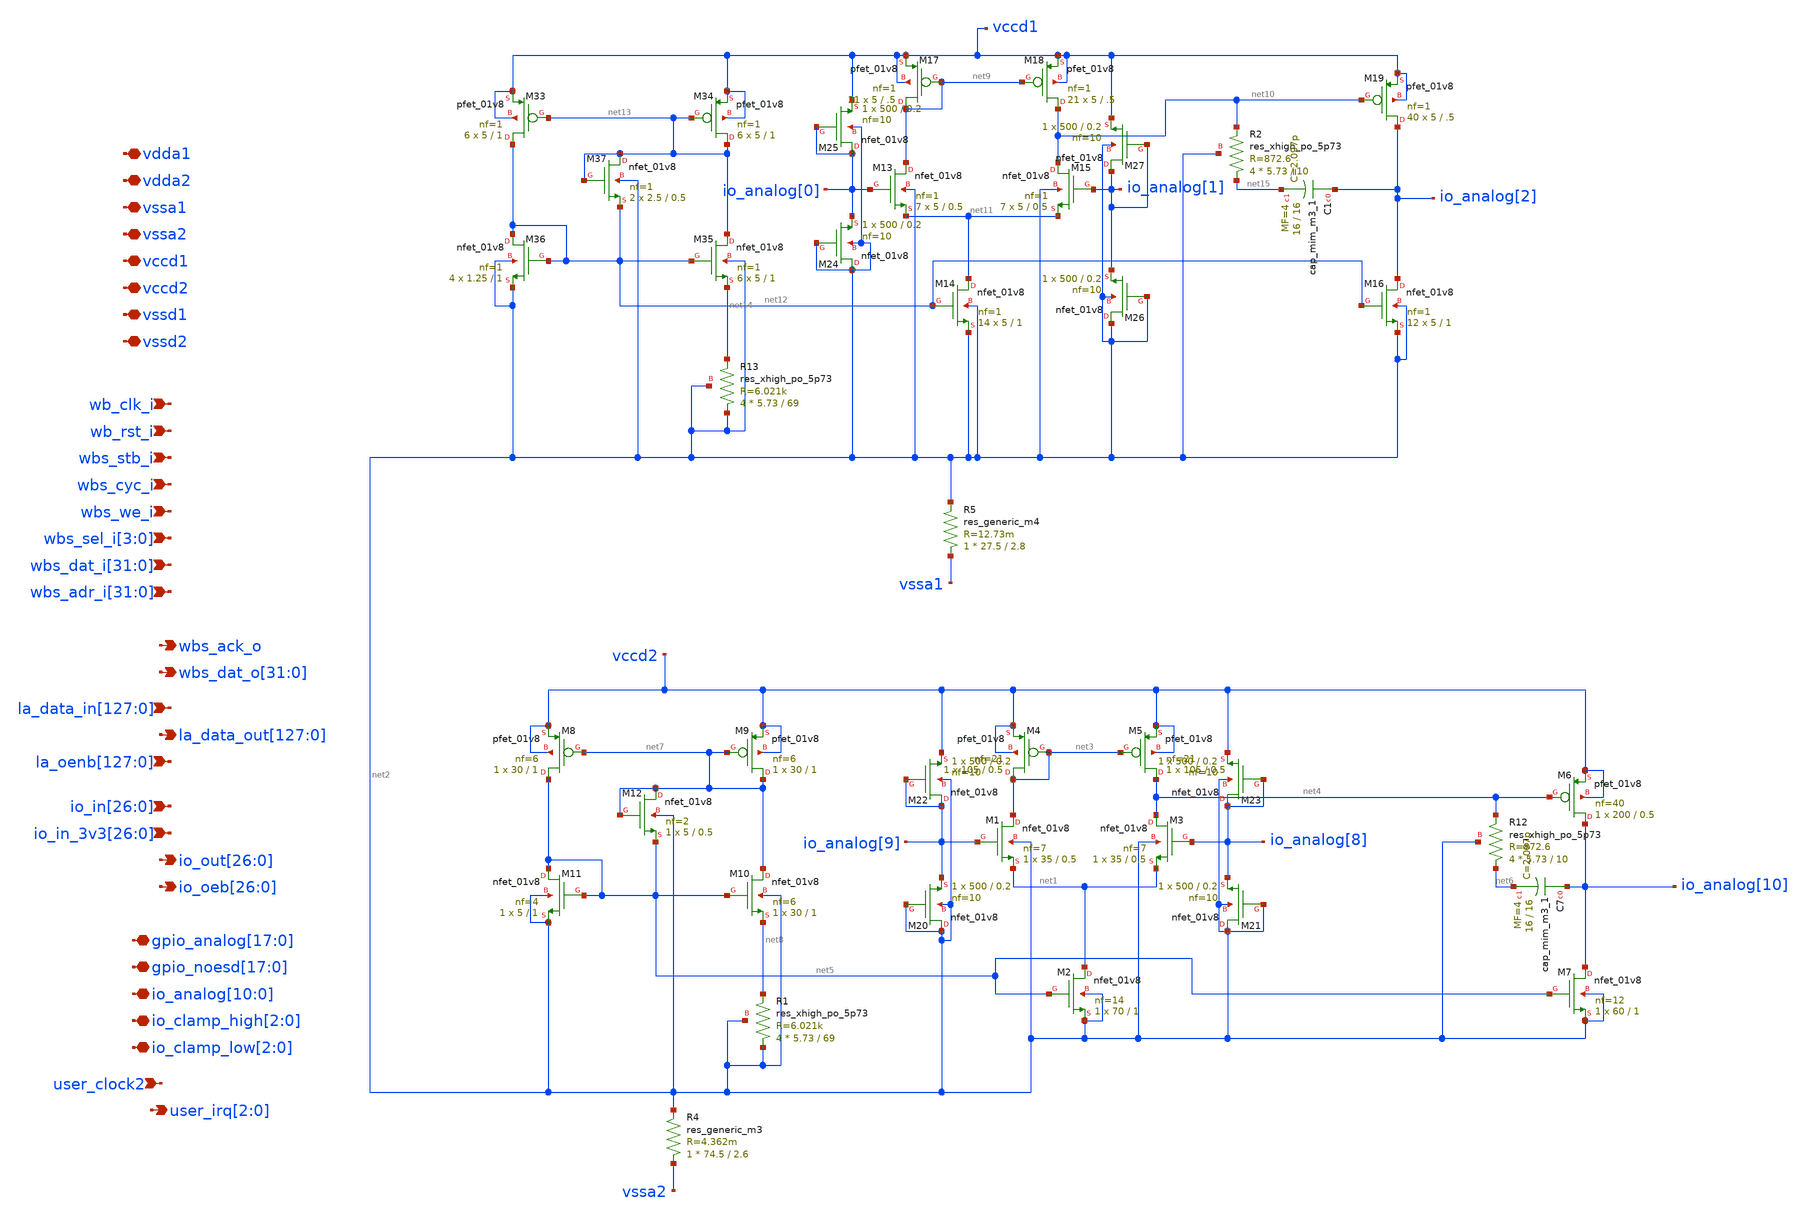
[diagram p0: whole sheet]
** sch_path: xschem/user_analog_project_wrapper.sch
**.subckt user_analog_project_wrapper vdda1 vdda2 vssa1 vssa2 vccd1 vccd2 vssd1 vssd2 wb_clk_i
*+ wb_rst_i wbs_stb_i wbs_cyc_i wbs_we_i wbs_sel_i[3],wbs_sel_i[2],wbs_sel_i[1],wbs_sel_i[0]
*+ wbs_dat_i[31],wbs_dat_i[30],wbs_dat_i[29],wbs_dat_i[28],wbs_dat_i[27],wbs_dat_i[26],wbs_dat_i[25],wbs_dat_i[24],wbs_dat_i[23],wbs_dat_i[22],wbs_dat_i[21],wbs_dat_i[20],wbs_dat_i[19],wbs_dat_i[18],wbs_dat_i[17],wbs_dat_i[16],wbs_dat_i[15],wbs_dat_i[14],wbs_dat_i[13],wbs_dat_i[12],wbs_dat_i[11],wbs_dat_i[10],wbs_dat_i[9],wbs_dat_i[8],wbs_dat_i[7],wbs_dat_i[6],wbs_dat_i[5],wbs_dat_i[4],wbs_dat_i[3],wbs_dat_i[2],wbs_dat_i[1],wbs_dat_i[0]
*+ wbs_adr_i[31],wbs_adr_i[30],wbs_adr_i[29],wbs_adr_i[28],wbs_adr_i[27],wbs_adr_i[26],wbs_adr_i[25],wbs_adr_i[24],wbs_adr_i[23],wbs_adr_i[22],wbs_adr_i[21],wbs_adr_i[20],wbs_adr_i[19],wbs_adr_i[18],wbs_adr_i[17],wbs_adr_i[16],wbs_adr_i[15],wbs_adr_i[14],wbs_adr_i[13],wbs_adr_i[12],wbs_adr_i[11],wbs_adr_i[10],wbs_adr_i[9],wbs_adr_i[8],wbs_adr_i[7],wbs_adr_i[6],wbs_adr_i[5],wbs_adr_i[4],wbs_adr_i[3],wbs_adr_i[2],wbs_adr_i[1],wbs_adr_i[0] wbs_ack_o
*+ wbs_dat_o[31],wbs_dat_o[30],wbs_dat_o[29],wbs_dat_o[28],wbs_dat_o[27],wbs_dat_o[26],wbs_dat_o[25],wbs_dat_o[24],wbs_dat_o[23],wbs_dat_o[22],wbs_dat_o[21],wbs_dat_o[20],wbs_dat_o[19],wbs_dat_o[18],wbs_dat_o[17],wbs_dat_o[16],wbs_dat_o[15],wbs_dat_o[14],wbs_dat_o[13],wbs_dat_o[12],wbs_dat_o[11],wbs_dat_o[10],wbs_dat_o[9],wbs_dat_o[8],wbs_dat_o[7],wbs_dat_o[6],wbs_dat_o[5],wbs_dat_o[4],wbs_dat_o[3],wbs_dat_o[2],wbs_dat_o[1],wbs_dat_o[0]
*+ la_data_in[127],la_data_in[126],la_data_in[125],la_data_in[124],la_data_in[123],la_data_in[122],la_data_in[121],la_data_in[120],la_data_in[119],la_data_in[118],la_data_in[117],la_data_in[116],la_data_in[115],la_data_in[114],la_data_in[113],la_data_in[112],la_data_in[111],la_data_in[110],la_data_in[109],la_data_in[108],la_data_in[107],la_data_in[106],la_data_in[105],la_data_in[104],la_data_in[103],la_data_in[102],la_data_in[101],la_data_in[100],la_data_in[99],la_data_in[98],la_data_in[97],la_data_in[96],la_data_in[95],la_data_in[94],la_data_in[93],la_data_in[92],la_data_in[91],la_data_in[90],la_data_in[89],la_data_in[88],la_data_in[87],la_data_in[86],la_data_in[85],la_data_in[84],la_data_in[83],la_data_in[82],la_data_in[81],la_data_in[80],la_data_in[79],la_data_in[78],la_data_in[77],la_data_in[76],la_data_in[75],la_data_in[74],la_data_in[73],la_data_in[72],la_data_in[71],la_data_in[70],la_data_in[69],la_data_in[68],la_data_in[67],la_data_in[66],la_data_in[65],la_data_in[64],la_data_in[63],la_data_in[62],la_data_in[61],la_data_in[60],la_data_in[59],la_data_in[58],la_data_in[57],la_data_in[56],la_data_in[55],la_data_in[54],la_data_in[53],la_data_in[52],la_data_in[51],la_data_in[50],la_data_in[49],la_data_in[48],la_data_in[47],la_data_in[46],la_data_in[45],la_data_in[44],la_data_in[43],la_data_in[42],la_data_in[41],la_data_in[40],la_data_in[39],la_data_in[38],la_data_in[37],la_data_in[36],la_data_in[35],la_data_in[34],la_data_in[33],la_data_in[32],la_data_in[31],la_data_in[30],la_data_in[29],la_data_in[28],la_data_in[27],la_data_in[26],la_data_in[25],la_data_in[24],la_data_in[23],la_data_in[22],la_data_in[21],la_data_in[20],la_data_in[19],la_data_in[18],la_data_in[17],la_data_in[16],la_data_in[15],la_data_in[14],la_data_in[13],la_data_in[12],la_data_in[11],la_data_in[10],la_data_in[9],la_data_in[8],la_data_in[7],la_data_in[6],la_data_in[5],la_data_in[4],la_data_in[3],la_data_in[2],la_data_in[1],la_data_in[0]
*+ la_data_out[127],la_data_out[126],la_data_out[125],la_data_out[124],la_data_out[123],la_data_out[122],la_data_out[121],la_data_out[120],la_data_out[119],la_data_out[118],la_data_out[117],la_data_out[116],la_data_out[115],la_data_out[114],la_data_out[113],la_data_out[112],la_data_out[111],la_data_out[110],la_data_out[109],la_data_out[108],la_data_out[107],la_data_out[106],la_data_out[105],la_data_out[104],la_data_out[103],la_data_out[102],la_data_out[101],la_data_out[100],la_data_out[99],la_data_out[98],la_data_out[97],la_data_out[96],la_data_out[95],la_data_out[94],la_data_out[93],la_data_out[92],la_data_out[91],la_data_out[90],la_data_out[89],la_data_out[88],la_data_out[87],la_data_out[86],la_data_out[85],la_data_out[84],la_data_out[83],la_data_out[82],la_data_out[81],la_data_out[80],la_data_out[79],la_data_out[78],la_data_out[77],la_data_out[76],la_data_out[75],la_data_out[74],la_data_out[73],la_data_out[72],la_data_out[71],la_data_out[70],la_data_out[69],la_data_out[68],la_data_out[67],la_data_out[66],la_data_out[65],la_data_out[64],la_data_out[63],la_data_out[62],la_data_out[61],la_data_out[60],la_data_out[59],la_data_out[58],la_data_out[57],la_data_out[56],la_data_out[55],la_data_out[54],la_data_out[53],la_data_out[52],la_data_out[51],la_data_out[50],la_data_out[49],la_data_out[48],la_data_out[47],la_data_out[46],la_data_out[45],la_data_out[44],la_data_out[43],la_data_out[42],la_data_out[41],la_data_out[40],la_data_out[39],la_data_out[38],la_data_out[37],la_data_out[36],la_data_out[35],la_data_out[34],la_data_out[33],la_data_out[32],la_data_out[31],la_data_out[30],la_data_out[29],la_data_out[28],la_data_out[27],la_data_out[26],la_data_out[25],la_data_out[24],la_data_out[23],la_data_out[22],la_data_out[21],la_data_out[20],la_data_out[19],la_data_out[18],la_data_out[17],la_data_out[16],la_data_out[15],la_data_out[14],la_data_out[13],la_data_out[12],la_data_out[11],la_data_out[10],la_data_out[9],la_data_out[8],la_data_out[7],la_data_out[6],la_data_out[5],la_data_out[4],la_data_out[3],la_data_out[2],la_data_out[1],la_data_out[0]
*+ io_in[26],io_in[25],io_in[24],io_in[23],io_in[22],io_in[21],io_in[20],io_in[19],io_in[18],io_in[17],io_in[16],io_in[15],io_in[14],io_in[13],io_in[12],io_in[11],io_in[10],io_in[9],io_in[8],io_in[7],io_in[6],io_in[5],io_in[4],io_in[3],io_in[2],io_in[1],io_in[0]
*+ io_in_3v3[26],io_in_3v3[25],io_in_3v3[24],io_in_3v3[23],io_in_3v3[22],io_in_3v3[21],io_in_3v3[20],io_in_3v3[19],io_in_3v3[18],io_in_3v3[17],io_in_3v3[16],io_in_3v3[15],io_in_3v3[14],io_in_3v3[13],io_in_3v3[12],io_in_3v3[11],io_in_3v3[10],io_in_3v3[9],io_in_3v3[8],io_in_3v3[7],io_in_3v3[6],io_in_3v3[5],io_in_3v3[4],io_in_3v3[3],io_in_3v3[2],io_in_3v3[1],io_in_3v3[0] user_clock2
*+ io_out[26],io_out[25],io_out[24],io_out[23],io_out[22],io_out[21],io_out[20],io_out[19],io_out[18],io_out[17],io_out[16],io_out[15],io_out[14],io_out[13],io_out[12],io_out[11],io_out[10],io_out[9],io_out[8],io_out[7],io_out[6],io_out[5],io_out[4],io_out[3],io_out[2],io_out[1],io_out[0]
*+ io_oeb[26],io_oeb[25],io_oeb[24],io_oeb[23],io_oeb[22],io_oeb[21],io_oeb[20],io_oeb[19],io_oeb[18],io_oeb[17],io_oeb[16],io_oeb[15],io_oeb[14],io_oeb[13],io_oeb[12],io_oeb[11],io_oeb[10],io_oeb[9],io_oeb[8],io_oeb[7],io_oeb[6],io_oeb[5],io_oeb[4],io_oeb[3],io_oeb[2],io_oeb[1],io_oeb[0]
*+ gpio_analog[17],gpio_analog[16],gpio_analog[15],gpio_analog[14],gpio_analog[13],gpio_analog[12],gpio_analog[11],gpio_analog[10],gpio_analog[9],gpio_analog[8],gpio_analog[7],gpio_analog[6],gpio_analog[5],gpio_analog[4],gpio_analog[3],gpio_analog[2],gpio_analog[1],gpio_analog[0]
*+ gpio_noesd[17],gpio_noesd[16],gpio_noesd[15],gpio_noesd[14],gpio_noesd[13],gpio_noesd[12],gpio_noesd[11],gpio_noesd[10],gpio_noesd[9],gpio_noesd[8],gpio_noesd[7],gpio_noesd[6],gpio_noesd[5],gpio_noesd[4],gpio_noesd[3],gpio_noesd[2],gpio_noesd[1],gpio_noesd[0]
*+ io_analog[10],io_analog[9],io_analog[8],io_analog[7],io_analog[6],io_analog[5],io_analog[4],io_analog[3],io_analog[2],io_analog[1],io_analog[0] io_clamp_high[2],io_clamp_high[1],io_clamp_high[0] io_clamp_low[2],io_clamp_low[1],io_clamp_low[0]
*+ user_irq[2],user_irq[1],user_irq[0]
*+ la_oenb[127],la_oenb[126],la_oenb[125],la_oenb[124],la_oenb[123],la_oenb[122],la_oenb[121],la_oenb[120],la_oenb[119],la_oenb[118],la_oenb[117],la_oenb[116],la_oenb[115],la_oenb[114],la_oenb[113],la_oenb[112],la_oenb[111],la_oenb[110],la_oenb[109],la_oenb[108],la_oenb[107],la_oenb[106],la_oenb[105],la_oenb[104],la_oenb[103],la_oenb[102],la_oenb[101],la_oenb[100],la_oenb[99],la_oenb[98],la_oenb[97],la_oenb[96],la_oenb[95],la_oenb[94],la_oenb[93],la_oenb[92],la_oenb[91],la_oenb[90],la_oenb[89],la_oenb[88],la_oenb[87],la_oenb[86],la_oenb[85],la_oenb[84],la_oenb[83],la_oenb[82],la_oenb[81],la_oenb[80],la_oenb[79],la_oenb[78],la_oenb[77],la_oenb[76],la_oenb[75],la_oenb[74],la_oenb[73],la_oenb[72],la_oenb[71],la_oenb[70],la_oenb[69],la_oenb[68],la_oenb[67],la_oenb[66],la_oenb[65],la_oenb[64],la_oenb[63],la_oenb[62],la_oenb[61],la_oenb[60],la_oenb[59],la_oenb[58],la_oenb[57],la_oenb[56],la_oenb[55],la_oenb[54],la_oenb[53],la_oenb[52],la_oenb[51],la_oenb[50],la_oenb[49],la_oenb[48],la_oenb[47],la_oenb[46],la_oenb[45],la_oenb[44],la_oenb[43],la_oenb[42],la_oenb[41],la_oenb[40],la_oenb[39],la_oenb[38],la_oenb[37],la_oenb[36],la_oenb[35],la_oenb[34],la_oenb[33],la_oenb[32],la_oenb[31],la_oenb[30],la_oenb[29],la_oenb[28],la_oenb[27],la_oenb[26],la_oenb[25],la_oenb[24],la_oenb[23],la_oenb[22],la_oenb[21],la_oenb[20],la_oenb[19],la_oenb[18],la_oenb[17],la_oenb[16],la_oenb[15],la_oenb[14],la_oenb[13],la_oenb[12],la_oenb[11],la_oenb[10],la_oenb[9],la_oenb[8],la_oenb[7],la_oenb[6],la_oenb[5],la_oenb[4],la_oenb[3],la_oenb[2],la_oenb[1],la_oenb[0]
*.iopin vdda1
*.iopin vdda2
*.iopin vssa1
*.iopin vssa2
*.iopin vccd1
*.iopin vccd2
*.iopin vssd1
*.iopin vssd2
*.ipin wb_clk_i
*.ipin wb_rst_i
*.ipin wbs_stb_i
*.ipin wbs_cyc_i
*.ipin wbs_we_i
*.ipin wbs_sel_i[3],wbs_sel_i[2],wbs_sel_i[1],wbs_sel_i[0]
*.ipin
*+ wbs_dat_i[31],wbs_dat_i[30],wbs_dat_i[29],wbs_dat_i[28],wbs_dat_i[27],wbs_dat_i[26],wbs_dat_i[25],wbs_dat_i[24],wbs_dat_i[23],wbs_dat_i[22],wbs_dat_i[21],wbs_dat_i[20],wbs_dat_i[19],wbs_dat_i[18],wbs_dat_i[17],wbs_dat_i[16],wbs_dat_i[15],wbs_dat_i[14],wbs_dat_i[13],wbs_dat_i[12],wbs_dat_i[11],wbs_dat_i[10],wbs_dat_i[9],wbs_dat_i[8],wbs_dat_i[7],wbs_dat_i[6],wbs_dat_i[5],wbs_dat_i[4],wbs_dat_i[3],wbs_dat_i[2],wbs_dat_i[1],wbs_dat_i[0]
*.ipin
*+ wbs_adr_i[31],wbs_adr_i[30],wbs_adr_i[29],wbs_adr_i[28],wbs_adr_i[27],wbs_adr_i[26],wbs_adr_i[25],wbs_adr_i[24],wbs_adr_i[23],wbs_adr_i[22],wbs_adr_i[21],wbs_adr_i[20],wbs_adr_i[19],wbs_adr_i[18],wbs_adr_i[17],wbs_adr_i[16],wbs_adr_i[15],wbs_adr_i[14],wbs_adr_i[13],wbs_adr_i[12],wbs_adr_i[11],wbs_adr_i[10],wbs_adr_i[9],wbs_adr_i[8],wbs_adr_i[7],wbs_adr_i[6],wbs_adr_i[5],wbs_adr_i[4],wbs_adr_i[3],wbs_adr_i[2],wbs_adr_i[1],wbs_adr_i[0]
*.opin wbs_ack_o
*.opin
*+ wbs_dat_o[31],wbs_dat_o[30],wbs_dat_o[29],wbs_dat_o[28],wbs_dat_o[27],wbs_dat_o[26],wbs_dat_o[25],wbs_dat_o[24],wbs_dat_o[23],wbs_dat_o[22],wbs_dat_o[21],wbs_dat_o[20],wbs_dat_o[19],wbs_dat_o[18],wbs_dat_o[17],wbs_dat_o[16],wbs_dat_o[15],wbs_dat_o[14],wbs_dat_o[13],wbs_dat_o[12],wbs_dat_o[11],wbs_dat_o[10],wbs_dat_o[9],wbs_dat_o[8],wbs_dat_o[7],wbs_dat_o[6],wbs_dat_o[5],wbs_dat_o[4],wbs_dat_o[3],wbs_dat_o[2],wbs_dat_o[1],wbs_dat_o[0]
*.ipin
*+ la_data_in[127],la_data_in[126],la_data_in[125],la_data_in[124],la_data_in[123],la_data_in[122],la_data_in[121],la_data_in[120],la_data_in[119],la_data_in[118],la_data_in[117],la_data_in[116],la_data_in[115],la_data_in[114],la_data_in[113],la_data_in[112],la_data_in[111],la_data_in[110],la_data_in[109],la_data_in[108],la_data_in[107],la_data_in[106],la_data_in[105],la_data_in[104],la_data_in[103],la_data_in[102],la_data_in[101],la_data_in[100],la_data_in[99],la_data_in[98],la_data_in[97],la_data_in[96],la_data_in[95],la_data_in[94],la_data_in[93],la_data_in[92],la_data_in[91],la_data_in[90],la_data_in[89],la_data_in[88],la_data_in[87],la_data_in[86],la_data_in[85],la_data_in[84],la_data_in[83],la_data_in[82],la_data_in[81],la_data_in[80],la_data_in[79],la_data_in[78],la_data_in[77],la_data_in[76],la_data_in[75],la_data_in[74],la_data_in[73],la_data_in[72],la_data_in[71],la_data_in[70],la_data_in[69],la_data_in[68],la_data_in[67],la_data_in[66],la_data_in[65],la_data_in[64],la_data_in[63],la_data_in[62],la_data_in[61],la_data_in[60],la_data_in[59],la_data_in[58],la_data_in[57],la_data_in[56],la_data_in[55],la_data_in[54],la_data_in[53],la_data_in[52],la_data_in[51],la_data_in[50],la_data_in[49],la_data_in[48],la_data_in[47],la_data_in[46],la_data_in[45],la_data_in[44],la_data_in[43],la_data_in[42],la_data_in[41],la_data_in[40],la_data_in[39],la_data_in[38],la_data_in[37],la_data_in[36],la_data_in[35],la_data_in[34],la_data_in[33],la_data_in[32],la_data_in[31],la_data_in[30],la_data_in[29],la_data_in[28],la_data_in[27],la_data_in[26],la_data_in[25],la_data_in[24],la_data_in[23],la_data_in[22],la_data_in[21],la_data_in[20],la_data_in[19],la_data_in[18],la_data_in[17],la_data_in[16],la_data_in[15],la_data_in[14],la_data_in[13],la_data_in[12],la_data_in[11],la_data_in[10],la_data_in[9],la_data_in[8],la_data_in[7],la_data_in[6],la_data_in[5],la_data_in[4],la_data_in[3],la_data_in[2],la_data_in[1],la_data_in[0]
*.opin
*+ la_data_out[127],la_data_out[126],la_data_out[125],la_data_out[124],la_data_out[123],la_data_out[122],la_data_out[121],la_data_out[120],la_data_out[119],la_data_out[118],la_data_out[117],la_data_out[116],la_data_out[115],la_data_out[114],la_data_out[113],la_data_out[112],la_data_out[111],la_data_out[110],la_data_out[109],la_data_out[108],la_data_out[107],la_data_out[106],la_data_out[105],la_data_out[104],la_data_out[103],la_data_out[102],la_data_out[101],la_data_out[100],la_data_out[99],la_data_out[98],la_data_out[97],la_data_out[96],la_data_out[95],la_data_out[94],la_data_out[93],la_data_out[92],la_data_out[91],la_data_out[90],la_data_out[89],la_data_out[88],la_data_out[87],la_data_out[86],la_data_out[85],la_data_out[84],la_data_out[83],la_data_out[82],la_data_out[81],la_data_out[80],la_data_out[79],la_data_out[78],la_data_out[77],la_data_out[76],la_data_out[75],la_data_out[74],la_data_out[73],la_data_out[72],la_data_out[71],la_data_out[70],la_data_out[69],la_data_out[68],la_data_out[67],la_data_out[66],la_data_out[65],la_data_out[64],la_data_out[63],la_data_out[62],la_data_out[61],la_data_out[60],la_data_out[59],la_data_out[58],la_data_out[57],la_data_out[56],la_data_out[55],la_data_out[54],la_data_out[53],la_data_out[52],la_data_out[51],la_data_out[50],la_data_out[49],la_data_out[48],la_data_out[47],la_data_out[46],la_data_out[45],la_data_out[44],la_data_out[43],la_data_out[42],la_data_out[41],la_data_out[40],la_data_out[39],la_data_out[38],la_data_out[37],la_data_out[36],la_data_out[35],la_data_out[34],la_data_out[33],la_data_out[32],la_data_out[31],la_data_out[30],la_data_out[29],la_data_out[28],la_data_out[27],la_data_out[26],la_data_out[25],la_data_out[24],la_data_out[23],la_data_out[22],la_data_out[21],la_data_out[20],la_data_out[19],la_data_out[18],la_data_out[17],la_data_out[16],la_data_out[15],la_data_out[14],la_data_out[13],la_data_out[12],la_data_out[11],la_data_out[10],la_data_out[9],la_data_out[8],la_data_out[7],la_data_out[6],la_data_out[5],la_data_out[4],la_data_out[3],la_data_out[2],la_data_out[1],la_data_out[0]
*.ipin
*+ io_in[26],io_in[25],io_in[24],io_in[23],io_in[22],io_in[21],io_in[20],io_in[19],io_in[18],io_in[17],io_in[16],io_in[15],io_in[14],io_in[13],io_in[12],io_in[11],io_in[10],io_in[9],io_in[8],io_in[7],io_in[6],io_in[5],io_in[4],io_in[3],io_in[2],io_in[1],io_in[0]
*.ipin
*+ io_in_3v3[26],io_in_3v3[25],io_in_3v3[24],io_in_3v3[23],io_in_3v3[22],io_in_3v3[21],io_in_3v3[20],io_in_3v3[19],io_in_3v3[18],io_in_3v3[17],io_in_3v3[16],io_in_3v3[15],io_in_3v3[14],io_in_3v3[13],io_in_3v3[12],io_in_3v3[11],io_in_3v3[10],io_in_3v3[9],io_in_3v3[8],io_in_3v3[7],io_in_3v3[6],io_in_3v3[5],io_in_3v3[4],io_in_3v3[3],io_in_3v3[2],io_in_3v3[1],io_in_3v3[0]
*.ipin user_clock2
*.opin
*+ io_out[26],io_out[25],io_out[24],io_out[23],io_out[22],io_out[21],io_out[20],io_out[19],io_out[18],io_out[17],io_out[16],io_out[15],io_out[14],io_out[13],io_out[12],io_out[11],io_out[10],io_out[9],io_out[8],io_out[7],io_out[6],io_out[5],io_out[4],io_out[3],io_out[2],io_out[1],io_out[0]
*.opin
*+ io_oeb[26],io_oeb[25],io_oeb[24],io_oeb[23],io_oeb[22],io_oeb[21],io_oeb[20],io_oeb[19],io_oeb[18],io_oeb[17],io_oeb[16],io_oeb[15],io_oeb[14],io_oeb[13],io_oeb[12],io_oeb[11],io_oeb[10],io_oeb[9],io_oeb[8],io_oeb[7],io_oeb[6],io_oeb[5],io_oeb[4],io_oeb[3],io_oeb[2],io_oeb[1],io_oeb[0]
*.iopin
*+ gpio_analog[17],gpio_analog[16],gpio_analog[15],gpio_analog[14],gpio_analog[13],gpio_analog[12],gpio_analog[11],gpio_analog[10],gpio_analog[9],gpio_analog[8],gpio_analog[7],gpio_analog[6],gpio_analog[5],gpio_analog[4],gpio_analog[3],gpio_analog[2],gpio_analog[1],gpio_analog[0]
*.iopin
*+ gpio_noesd[17],gpio_noesd[16],gpio_noesd[15],gpio_noesd[14],gpio_noesd[13],gpio_noesd[12],gpio_noesd[11],gpio_noesd[10],gpio_noesd[9],gpio_noesd[8],gpio_noesd[7],gpio_noesd[6],gpio_noesd[5],gpio_noesd[4],gpio_noesd[3],gpio_noesd[2],gpio_noesd[1],gpio_noesd[0]
*.iopin
*+ io_analog[10],io_analog[9],io_analog[8],io_analog[7],io_analog[6],io_analog[5],io_analog[4],io_analog[3],io_analog[2],io_analog[1],io_analog[0]
*.iopin io_clamp_high[2],io_clamp_high[1],io_clamp_high[0]
*.iopin io_clamp_low[2],io_clamp_low[1],io_clamp_low[0]
*.opin user_irq[2],user_irq[1],user_irq[0]
*.ipin
*+ la_oenb[127],la_oenb[126],la_oenb[125],la_oenb[124],la_oenb[123],la_oenb[122],la_oenb[121],la_oenb[120],la_oenb[119],la_oenb[118],la_oenb[117],la_oenb[116],la_oenb[115],la_oenb[114],la_oenb[113],la_oenb[112],la_oenb[111],la_oenb[110],la_oenb[109],la_oenb[108],la_oenb[107],la_oenb[106],la_oenb[105],la_oenb[104],la_oenb[103],la_oenb[102],la_oenb[101],la_oenb[100],la_oenb[99],la_oenb[98],la_oenb[97],la_oenb[96],la_oenb[95],la_oenb[94],la_oenb[93],la_oenb[92],la_oenb[91],la_oenb[90],la_oenb[89],la_oenb[88],la_oenb[87],la_oenb[86],la_oenb[85],la_oenb[84],la_oenb[83],la_oenb[82],la_oenb[81],la_oenb[80],la_oenb[79],la_oenb[78],la_oenb[77],la_oenb[76],la_oenb[75],la_oenb[74],la_oenb[73],la_oenb[72],la_oenb[71],la_oenb[70],la_oenb[69],la_oenb[68],la_oenb[67],la_oenb[66],la_oenb[65],la_oenb[64],la_oenb[63],la_oenb[62],la_oenb[61],la_oenb[60],la_oenb[59],la_oenb[58],la_oenb[57],la_oenb[56],la_oenb[55],la_oenb[54],la_oenb[53],la_oenb[52],la_oenb[51],la_oenb[50],la_oenb[49],la_oenb[48],la_oenb[47],la_oenb[46],la_oenb[45],la_oenb[44],la_oenb[43],la_oenb[42],la_oenb[41],la_oenb[40],la_oenb[39],la_oenb[38],la_oenb[37],la_oenb[36],la_oenb[35],la_oenb[34],la_oenb[33],la_oenb[32],la_oenb[31],la_oenb[30],la_oenb[29],la_oenb[28],la_oenb[27],la_oenb[26],la_oenb[25],la_oenb[24],la_oenb[23],la_oenb[22],la_oenb[21],la_oenb[20],la_oenb[19],la_oenb[18],la_oenb[17],la_oenb[16],la_oenb[15],la_oenb[14],la_oenb[13],la_oenb[12],la_oenb[11],la_oenb[10],la_oenb[9],la_oenb[8],la_oenb[7],la_oenb[6],la_oenb[5],la_oenb[4],la_oenb[3],la_oenb[2],la_oenb[1],la_oenb[0]
XM2 net1 net5 net2 net2 sky130_fd_pr__nfet_01v8 L=1 W=70 nf=14 ad='int((nf+1)/2) * W/nf * 0.29' as='int((nf+2)/2) * W/nf * 0.29'
+ pd='2*int((nf+1)/2) * (W/nf + 0.29)' ps='2*int((nf+2)/2) * (W/nf + 0.29)' nrd='0.29 / W' nrs='0.29 / W'
+ sa=0 sb=0 sd=0 mult=1 m=1
XM1 net3 io_analog[9] net1 net2 sky130_fd_pr__nfet_01v8 L=0.5 W=35 nf=7 ad='int((nf+1)/2) * W/nf * 0.29'
+ as='int((nf+2)/2) * W/nf * 0.29' pd='2*int((nf+1)/2) * (W/nf + 0.29)' ps='2*int((nf+2)/2) * (W/nf + 0.29)'
+ nrd='0.29 / W' nrs='0.29 / W' sa=0 sb=0 sd=0 mult=1 m=1
XM3 net4 io_analog[8] net1 net2 sky130_fd_pr__nfet_01v8 L=0.5 W=35 nf=7 ad='int((nf+1)/2) * W/nf * 0.29'
+ as='int((nf+2)/2) * W/nf * 0.29' pd='2*int((nf+1)/2) * (W/nf + 0.29)' ps='2*int((nf+2)/2) * (W/nf + 0.29)'
+ nrd='0.29 / W' nrs='0.29 / W' sa=0 sb=0 sd=0 mult=1 m=1
XM4 net3 net3 vccd2 vccd2 sky130_fd_pr__pfet_01v8 L=0.5 W=105 nf=21 ad='int((nf+1)/2) * W/nf * 0.29'
+ as='int((nf+2)/2) * W/nf * 0.29' pd='2*int((nf+1)/2) * (W/nf + 0.29)' ps='2*int((nf+2)/2) * (W/nf + 0.29)'
+ nrd='0.29 / W' nrs='0.29 / W' sa=0 sb=0 sd=0 mult=1 m=1
XM5 net4 net3 vccd2 vccd2 sky130_fd_pr__pfet_01v8 L=0.5 W=105 nf=21 ad='int((nf+1)/2) * W/nf * 0.29'
+ as='int((nf+2)/2) * W/nf * 0.29' pd='2*int((nf+1)/2) * (W/nf + 0.29)' ps='2*int((nf+2)/2) * (W/nf + 0.29)'
+ nrd='0.29 / W' nrs='0.29 / W' sa=0 sb=0 sd=0 mult=1 m=1
XM6 io_analog[10] net4 vccd2 vccd2 sky130_fd_pr__pfet_01v8 L=0.5 W=200 nf=40 ad='int((nf+1)/2) * W/nf * 0.29'
+ as='int((nf+2)/2) * W/nf * 0.29' pd='2*int((nf+1)/2) * (W/nf + 0.29)' ps='2*int((nf+2)/2) * (W/nf + 0.29)'
+ nrd='0.29 / W' nrs='0.29 / W' sa=0 sb=0 sd=0 mult=1 m=1
XM7 io_analog[10] net5 net2 net2 sky130_fd_pr__nfet_01v8 L=1 W=60 nf=12 ad='int((nf+1)/2) * W/nf * 0.29'
+ as='int((nf+2)/2) * W/nf * 0.29' pd='2*int((nf+1)/2) * (W/nf + 0.29)' ps='2*int((nf+2)/2) * (W/nf + 0.29)'
+ nrd='0.29 / W' nrs='0.29 / W' sa=0 sb=0 sd=0 mult=1 m=1
XC7 io_analog[10] net6 sky130_fd_pr__cap_mim_m3_1 W=16 L=16 MF=4 m=4
XR12 net6 net4 net2 sky130_fd_pr__res_xhigh_po_5p73 L=10 mult=4 m=4
XM8 net5 net7 vccd2 vccd2 sky130_fd_pr__pfet_01v8 L=1 W=30 nf=6 ad='int((nf+1)/2) * W/nf * 0.29' as='int((nf+2)/2) * W/nf * 0.29'
+ pd='2*int((nf+1)/2) * (W/nf + 0.29)' ps='2*int((nf+2)/2) * (W/nf + 0.29)' nrd='0.29 / W' nrs='0.29 / W'
+ sa=0 sb=0 sd=0 mult=1 m=1
XM9 net7 net7 vccd2 vccd2 sky130_fd_pr__pfet_01v8 L=1 W=30 nf=6 ad='int((nf+1)/2) * W/nf * 0.29' as='int((nf+2)/2) * W/nf * 0.29'
+ pd='2*int((nf+1)/2) * (W/nf + 0.29)' ps='2*int((nf+2)/2) * (W/nf + 0.29)' nrd='0.29 / W' nrs='0.29 / W'
+ sa=0 sb=0 sd=0 mult=1 m=1
XM10 net7 net5 net8 net2 sky130_fd_pr__nfet_01v8 L=1 W=30 nf=6 ad='int((nf+1)/2) * W/nf * 0.29' as='int((nf+2)/2) * W/nf * 0.29'
+ pd='2*int((nf+1)/2) * (W/nf + 0.29)' ps='2*int((nf+2)/2) * (W/nf + 0.29)' nrd='0.29 / W' nrs='0.29 / W'
+ sa=0 sb=0 sd=0 mult=1 m=1
XM11 net5 net5 net2 net2 sky130_fd_pr__nfet_01v8 L=1 W=5 nf=4 ad='int((nf+1)/2) * W/nf * 0.29' as='int((nf+2)/2) * W/nf * 0.29'
+ pd='2*int((nf+1)/2) * (W/nf + 0.29)' ps='2*int((nf+2)/2) * (W/nf + 0.29)' nrd='0.29 / W' nrs='0.29 / W'
+ sa=0 sb=0 sd=0 mult=1 m=1
XM12 net7 net7 net5 net2 sky130_fd_pr__nfet_01v8 L=0.5 W=5 nf=2 ad='int((nf+1)/2) * W/nf * 0.29' as='int((nf+2)/2) * W/nf * 0.29'
+ pd='2*int((nf+1)/2) * (W/nf + 0.29)' ps='2*int((nf+2)/2) * (W/nf + 0.29)' nrd='0.29 / W' nrs='0.29 / W'
+ sa=0 sb=0 sd=0 mult=1 m=1
XR1 net2 net8 net2 sky130_fd_pr__res_xhigh_po_5p73 L=69 mult=4 m=4
XM13 net9 io_analog[0] net11 net2 sky130_fd_pr__nfet_01v8 L=0.5 W=5 nf=1 ad='int((nf+1)/2) * W/nf * 0.29'
+ as='int((nf+2)/2) * W/nf * 0.29' pd='2*int((nf+1)/2) * (W/nf + 0.29)' ps='2*int((nf+2)/2) * (W/nf + 0.29)'
+ nrd='0.29 / W' nrs='0.29 / W' sa=0 sb=0 sd=0 mult=7 m=7
XM14 net11 net12 net2 net2 sky130_fd_pr__nfet_01v8 L=1 W=5 nf=1 ad='int((nf+1)/2) * W/nf * 0.29' as='int((nf+2)/2) * W/nf * 0.29'
+ pd='2*int((nf+1)/2) * (W/nf + 0.29)' ps='2*int((nf+2)/2) * (W/nf + 0.29)' nrd='0.29 / W' nrs='0.29 / W'
+ sa=0 sb=0 sd=0 mult=14 m=14
XM15 net10 io_analog[1] net11 net2 sky130_fd_pr__nfet_01v8 L=0.5 W=5 nf=1 ad='int((nf+1)/2) * W/nf * 0.29'
+ as='int((nf+2)/2) * W/nf * 0.29' pd='2*int((nf+1)/2) * (W/nf + 0.29)' ps='2*int((nf+2)/2) * (W/nf + 0.29)'
+ nrd='0.29 / W' nrs='0.29 / W' sa=0 sb=0 sd=0 mult=7 m=7
XM16 io_analog[2] net12 net2 net2 sky130_fd_pr__nfet_01v8 L=1 W=5 nf=1 ad='int((nf+1)/2) * W/nf * 0.29'
+ as='int((nf+2)/2) * W/nf * 0.29' pd='2*int((nf+1)/2) * (W/nf + 0.29)' ps='2*int((nf+2)/2) * (W/nf + 0.29)'
+ nrd='0.29 / W' nrs='0.29 / W' sa=0 sb=0 sd=0 mult=12 m=12
XM17 net9 net9 vccd1 vccd1 sky130_fd_pr__pfet_01v8 L=.5 W=5 nf=1 ad='int((nf+1)/2) * W/nf * 0.29' as='int((nf+2)/2) * W/nf * 0.29'
+ pd='2*int((nf+1)/2) * (W/nf + 0.29)' ps='2*int((nf+2)/2) * (W/nf + 0.29)' nrd='0.29 / W' nrs='0.29 / W'
+ sa=0 sb=0 sd=0 mult=21 m=21
XM18 net10 net9 vccd1 vccd1 sky130_fd_pr__pfet_01v8 L=.5 W=5 nf=1 ad='int((nf+1)/2) * W/nf * 0.29' as='int((nf+2)/2) * W/nf * 0.29'
+ pd='2*int((nf+1)/2) * (W/nf + 0.29)' ps='2*int((nf+2)/2) * (W/nf + 0.29)' nrd='0.29 / W' nrs='0.29 / W'
+ sa=0 sb=0 sd=0 mult=21 m=21
XM19 io_analog[2] net10 vccd1 vccd1 sky130_fd_pr__pfet_01v8 L=.5 W=5 nf=1 ad='int((nf+1)/2) * W/nf * 0.29'
+ as='int((nf+2)/2) * W/nf * 0.29' pd='2*int((nf+1)/2) * (W/nf + 0.29)' ps='2*int((nf+2)/2) * (W/nf + 0.29)'
+ nrd='0.29 / W' nrs='0.29 / W' sa=0 sb=0 sd=0 mult=40 m=40
XR2 net15 net10 net2 sky130_fd_pr__res_xhigh_po_5p73 L=10 mult=4 m=4
XC1 io_analog[2] net15 sky130_fd_pr__cap_mim_m3_1 W=16 L=16 MF=4 m=4
XM33 net12 net13 vccd1 vccd1 sky130_fd_pr__pfet_01v8 L=1 W=5 nf=1 ad='int((nf+1)/2) * W/nf * 0.29' as='int((nf+2)/2) * W/nf * 0.29'
+ pd='2*int((nf+1)/2) * (W/nf + 0.29)' ps='2*int((nf+2)/2) * (W/nf + 0.29)' nrd='0.29 / W' nrs='0.29 / W'
+ sa=0 sb=0 sd=0 mult=6 m=6
XM34 net13 net13 vccd1 vccd1 sky130_fd_pr__pfet_01v8 L=1 W=5 nf=1 ad='int((nf+1)/2) * W/nf * 0.29' as='int((nf+2)/2) * W/nf * 0.29'
+ pd='2*int((nf+1)/2) * (W/nf + 0.29)' ps='2*int((nf+2)/2) * (W/nf + 0.29)' nrd='0.29 / W' nrs='0.29 / W'
+ sa=0 sb=0 sd=0 mult=6 m=6
XM35 net13 net12 net14 net2 sky130_fd_pr__nfet_01v8 L=1 W=5 nf=1 ad='int((nf+1)/2) * W/nf * 0.29' as='int((nf+2)/2) * W/nf * 0.29'
+ pd='2*int((nf+1)/2) * (W/nf + 0.29)' ps='2*int((nf+2)/2) * (W/nf + 0.29)' nrd='0.29 / W' nrs='0.29 / W'
+ sa=0 sb=0 sd=0 mult=6 m=6
XM36 net12 net12 net2 net2 sky130_fd_pr__nfet_01v8 L=1 W=1.25 nf=1 ad='int((nf+1)/2) * W/nf * 0.29' as='int((nf+2)/2) * W/nf * 0.29'
+ pd='2*int((nf+1)/2) * (W/nf + 0.29)' ps='2*int((nf+2)/2) * (W/nf + 0.29)' nrd='0.29 / W' nrs='0.29 / W'
+ sa=0 sb=0 sd=0 mult=4 m=4
XM37 net13 net13 net12 net2 sky130_fd_pr__nfet_01v8 L=0.5 W=2.5 nf=1 ad='int((nf+1)/2) * W/nf * 0.29'
+ as='int((nf+2)/2) * W/nf * 0.29' pd='2*int((nf+1)/2) * (W/nf + 0.29)' ps='2*int((nf+2)/2) * (W/nf + 0.29)'
+ nrd='0.29 / W' nrs='0.29 / W' sa=0 sb=0 sd=0 mult=2 m=2
XR13 net2 net14 net2 sky130_fd_pr__res_xhigh_po_5p73 L=69 mult=4 m=4
R5 vssa1 net2 sky130_fd_pr__res_generic_m4 W=27.5 L=2.8 m=1
R4 vssa2 net2 sky130_fd_pr__res_generic_m3 W=74.5 L=2.6 m=1
XM20 net2 net2 io_analog[9] net2 sky130_fd_pr__nfet_01v8 L=0.2 W=500 nf=10 ad='int((nf+1)/2) * W/nf * 0.29'
+ as='int((nf+2)/2) * W/nf * 0.29' pd='2*int((nf+1)/2) * (W/nf + 0.29)' ps='2*int((nf+2)/2) * (W/nf + 0.29)'
+ nrd='0.29 / W' nrs='0.29 / W' sa=0 sb=0 sd=0 mult=1 m=1
XM21 net2 net2 io_analog[8] net2 sky130_fd_pr__nfet_01v8 L=0.2 W=500 nf=10 ad='int((nf+1)/2) * W/nf * 0.29'
+ as='int((nf+2)/2) * W/nf * 0.29' pd='2*int((nf+1)/2) * (W/nf + 0.29)' ps='2*int((nf+2)/2) * (W/nf + 0.29)'
+ nrd='0.29 / W' nrs='0.29 / W' sa=0 sb=0 sd=0 mult=1 m=1
XM22 io_analog[9] io_analog[9] vccd2 net2 sky130_fd_pr__nfet_01v8 L=0.2 W=500 nf=10 ad='int((nf+1)/2) * W/nf * 0.29'
+ as='int((nf+2)/2) * W/nf * 0.29' pd='2*int((nf+1)/2) * (W/nf + 0.29)' ps='2*int((nf+2)/2) * (W/nf + 0.29)'
+ nrd='0.29 / W' nrs='0.29 / W' sa=0 sb=0 sd=0 mult=1 m=1
XM23 io_analog[8] io_analog[8] vccd2 net2 sky130_fd_pr__nfet_01v8 L=0.2 W=500 nf=10 ad='int((nf+1)/2) * W/nf * 0.29'
+ as='int((nf+2)/2) * W/nf * 0.29' pd='2*int((nf+1)/2) * (W/nf + 0.29)' ps='2*int((nf+2)/2) * (W/nf + 0.29)'
+ nrd='0.29 / W' nrs='0.29 / W' sa=0 sb=0 sd=0 mult=1 m=1
XM24 net2 net2 io_analog[0] net2 sky130_fd_pr__nfet_01v8 L=0.2 W=500 nf=10 ad='int((nf+1)/2) * W/nf * 0.29'
+ as='int((nf+2)/2) * W/nf * 0.29' pd='2*int((nf+1)/2) * (W/nf + 0.29)' ps='2*int((nf+2)/2) * (W/nf + 0.29)'
+ nrd='0.29 / W' nrs='0.29 / W' sa=0 sb=0 sd=0 mult=1 m=1
XM25 io_analog[0] io_analog[0] vccd1 net2 sky130_fd_pr__nfet_01v8 L=0.2 W=500 nf=10 ad='int((nf+1)/2) * W/nf * 0.29'
+ as='int((nf+2)/2) * W/nf * 0.29' pd='2*int((nf+1)/2) * (W/nf + 0.29)' ps='2*int((nf+2)/2) * (W/nf + 0.29)'
+ nrd='0.29 / W' nrs='0.29 / W' sa=0 sb=0 sd=0 mult=1 m=1
XM26 net2 net2 io_analog[1] net2 sky130_fd_pr__nfet_01v8 L=0.2 W=500 nf=10 ad='int((nf+1)/2) * W/nf * 0.29'
+ as='int((nf+2)/2) * W/nf * 0.29' pd='2*int((nf+1)/2) * (W/nf + 0.29)' ps='2*int((nf+2)/2) * (W/nf + 0.29)'
+ nrd='0.29 / W' nrs='0.29 / W' sa=0 sb=0 sd=0 mult=1 m=1
XM27 io_analog[1] io_analog[1] vccd1 net2 sky130_fd_pr__nfet_01v8 L=0.2 W=500 nf=10 ad='int((nf+1)/2) * W/nf * 0.29'
+ as='int((nf+2)/2) * W/nf * 0.29' pd='2*int((nf+1)/2) * (W/nf + 0.29)' ps='2*int((nf+2)/2) * (W/nf + 0.29)'
+ nrd='0.29 / W' nrs='0.29 / W' sa=0 sb=0 sd=0 mult=1 m=1
**.ends
.end
